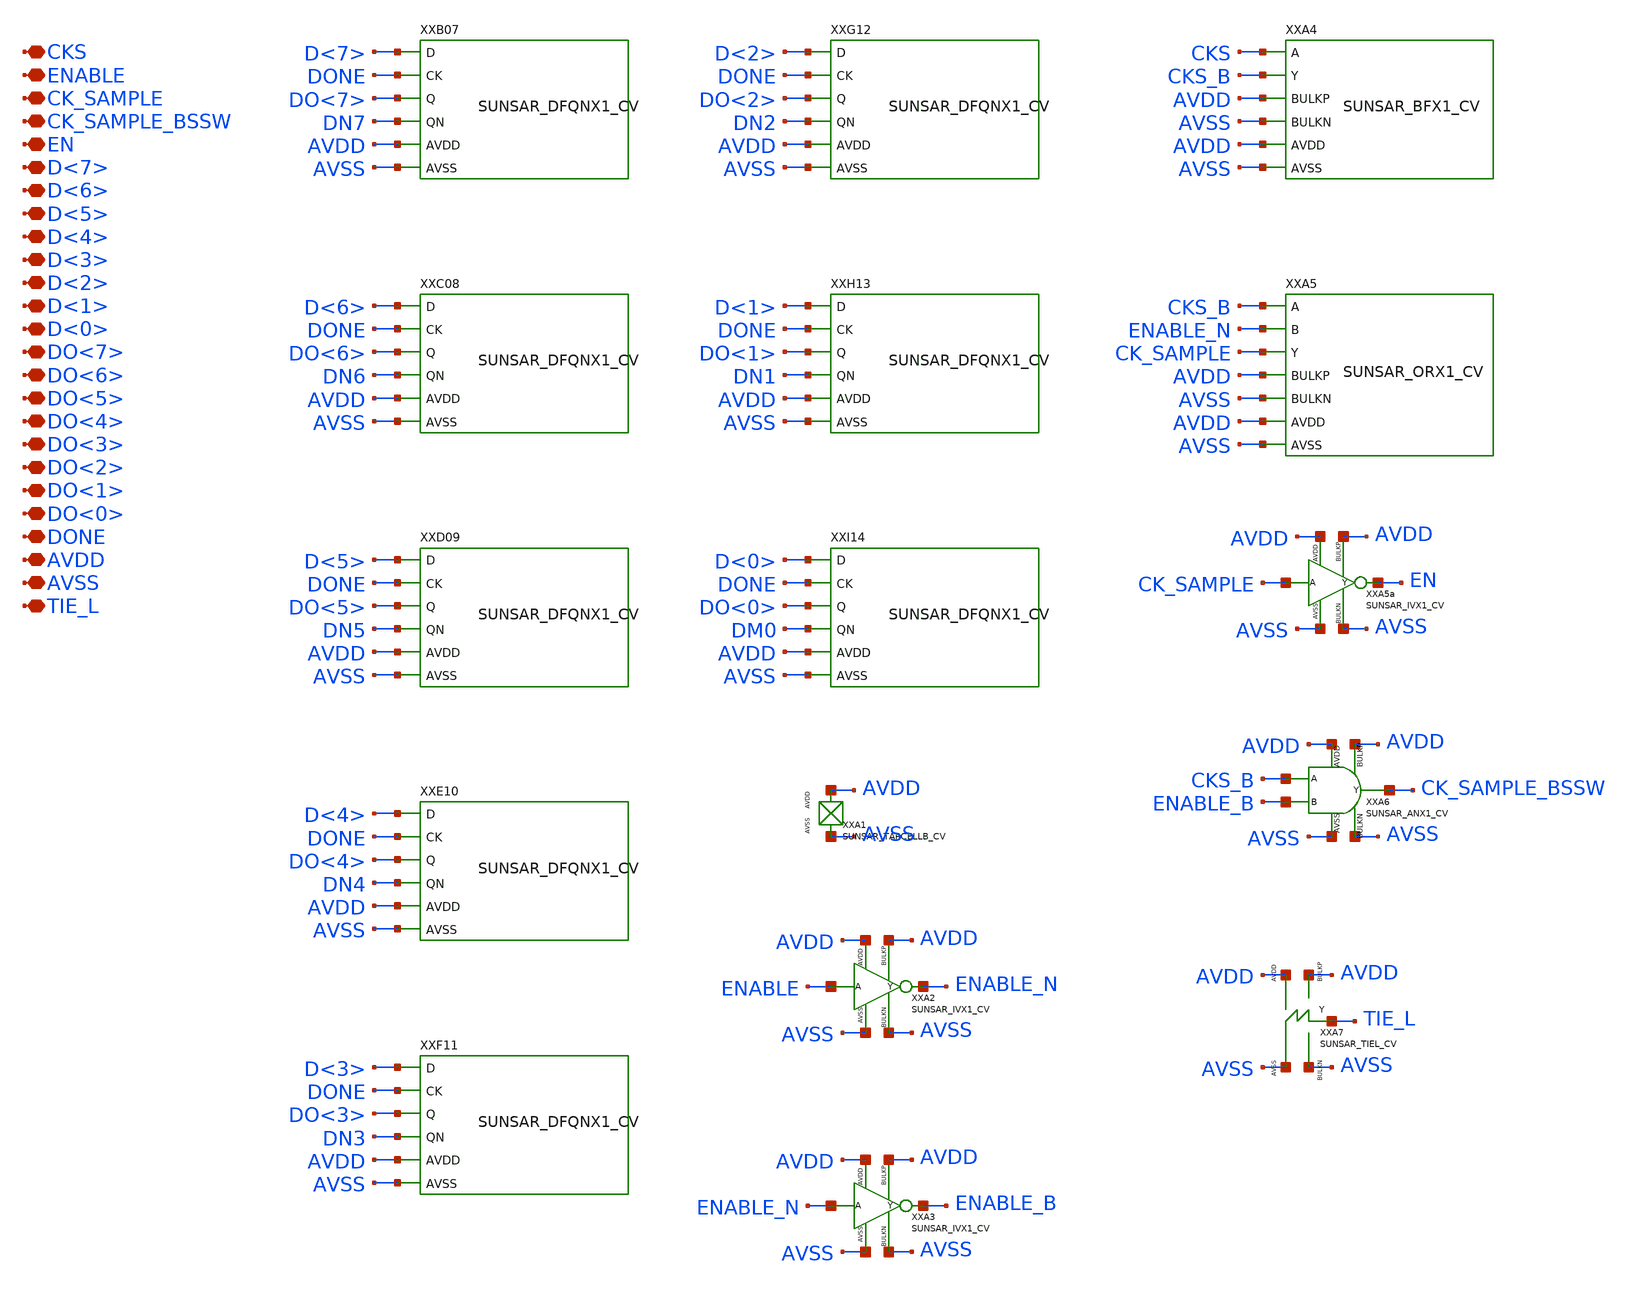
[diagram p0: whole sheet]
** sch_path: design/SUN_SAR9B_SKY130NM/SUNSAR_CAPT8B_CV.sch
**.subckt SUNSAR_CAPT8B_CV CKS ENABLE CK_SAMPLE CK_SAMPLE_BSSW EN D<7> D<6> D<5> D<4> D<3> D<2> D<1>
*+ D<0> DO<7> DO<6> DO<5> DO<4> DO<3> DO<2> DO<1> DO<0> DONE AVDD AVSS TIE_L
*.iopin CKS
*.iopin ENABLE
*.iopin CK_SAMPLE
*.iopin CK_SAMPLE_BSSW
*.iopin EN
*.iopin D<7>
*.iopin D<6>
*.iopin D<5>
*.iopin D<4>
*.iopin D<3>
*.iopin D<2>
*.iopin D<1>
*.iopin D<0>
*.iopin DO<7>
*.iopin DO<6>
*.iopin DO<5>
*.iopin DO<4>
*.iopin DO<3>
*.iopin DO<2>
*.iopin DO<1>
*.iopin DO<0>
*.iopin DONE
*.iopin AVDD
*.iopin AVSS
*.iopin TIE_L
XXB07 D<7> DONE DO<7> DN7 AVDD AVSS SUNSAR_DFQNX1_CV
XXC08 D<6> DONE DO<6> DN6 AVDD AVSS SUNSAR_DFQNX1_CV
XXD09 D<5> DONE DO<5> DN5 AVDD AVSS SUNSAR_DFQNX1_CV
XXE10 D<4> DONE DO<4> DN4 AVDD AVSS SUNSAR_DFQNX1_CV
XXF11 D<3> DONE DO<3> DN3 AVDD AVSS SUNSAR_DFQNX1_CV
XXG12 D<2> DONE DO<2> DN2 AVDD AVSS SUNSAR_DFQNX1_CV
XXH13 D<1> DONE DO<1> DN1 AVDD AVSS SUNSAR_DFQNX1_CV
XXI14 D<0> DONE DO<0> DM0 AVDD AVSS SUNSAR_DFQNX1_CV
XXA1 AVDD AVSS SUNSAR_TAPCELLB_CV
XXA2 ENABLE ENABLE_N AVDD AVSS AVDD AVSS SUNSAR_IVX1_CV
XXA3 ENABLE_N ENABLE_B AVDD AVSS AVDD AVSS SUNSAR_IVX1_CV
XXA4 CKS CKS_B AVDD AVSS AVDD AVSS SUNSAR_BFX1_CV
XXA5 CKS_B ENABLE_N CK_SAMPLE AVDD AVSS AVDD AVSS SUNSAR_ORX1_CV
XXA5a CK_SAMPLE EN AVDD AVSS AVDD AVSS SUNSAR_IVX1_CV
XXA6 CKS_B ENABLE_B CK_SAMPLE_BSSW AVDD AVSS AVSS AVDD SUNSAR_ANX1_CV
**.ends
.end
